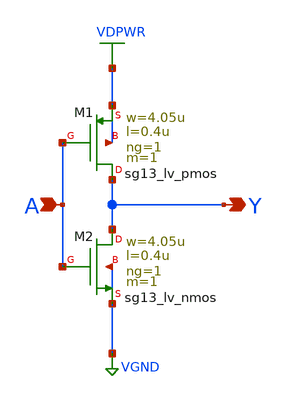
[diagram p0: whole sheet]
** sch_path: xschem/skullfet_inverter.sch
**.subckt skullfet_inverter A Y
*.ipin A
*.opin Y
XM1 Y A VDPWR VDPWR sg13_lv_pmos w=4.05u l=0.4u ng=1 m=1 mm_ok=1
XM2 Y A VGND VGND sg13_lv_nmos w=4.05u l=0.4u ng=1 m=1 mm_ok=1
**.ends
.GLOBAL VGND
.GLOBAL VDPWR
.end
